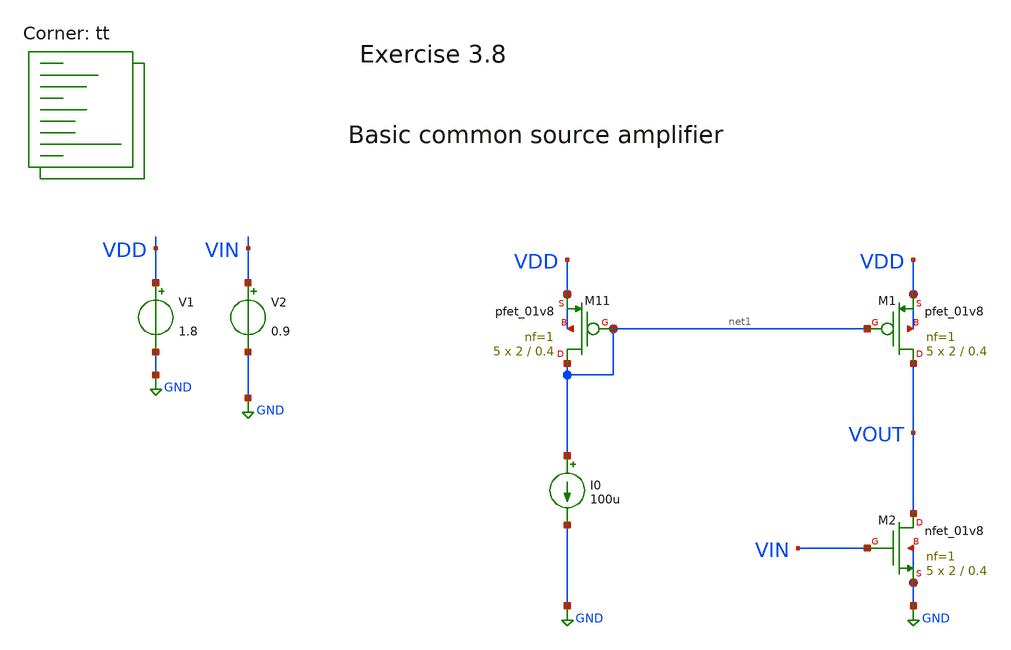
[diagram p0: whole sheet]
** sch_path: Analog_integrated_circuit_Design/chapter3/8/8.sch
**.subckt 8
V1 VDD GND 1.8
V2 VIN GND 0.9
XM11 net1 net1 VDD VDD sky130_fd_pr__pfet_01v8 L=0.4 W=2 nf=1 ad='int((nf+1)/2) * W/nf * 0.29' as='int((nf+2)/2) * W/nf * 0.29'
+ pd='2*int((nf+1)/2) * (W/nf + 0.29)' ps='2*int((nf+2)/2) * (W/nf + 0.29)' nrd='0.29 / W' nrs='0.29 / W'
+ sa=0 sb=0 sd=0 mult=5 m=5
I0 net1 GND 100u
XM1 VOUT net1 VDD VDD sky130_fd_pr__pfet_01v8 L=0.4 W=2 nf=1 ad='int((nf+1)/2) * W/nf * 0.29' as='int((nf+2)/2) * W/nf * 0.29'
+ pd='2*int((nf+1)/2) * (W/nf + 0.29)' ps='2*int((nf+2)/2) * (W/nf + 0.29)' nrd='0.29 / W' nrs='0.29 / W'
+ sa=0 sb=0 sd=0 mult=5 m=5
XM2 VOUT VIN GND GND sky130_fd_pr__nfet_01v8 L=0.4 W=2 nf=1 ad='int((1 + 1)/2) * 2 / 1 * 0.29' as='int((1 + 2)/2) * 2 / 1 * 0.29'
+ pd='2*int((1 + 1)/2) * (2 / 1 + 0.29)' ps='2*int((1 + 2)/2) * (2 / 1 + 0.29)' nrd='0.29 / 2 ' nrs='0.29 / 2 '
+ sa=0 sb=0 sd=0 mult=5 m=5
**** begin user architecture code
.lib $::SKYWATER_MODELS/sky130.lib.spice tt

**************************************************************
**************************************************************
**************************************************************
**************************************************************
**************************************************************
*LIBs*********************************************************
**************************************************************
**************************************************************
**************************************************************
**************************************************************
**************************************************************
*.lib $::SKYWATER_MODELS/sky130.lib.spice tt
* chose the corners in the corner file
* tt_mm for mismatch
* ss ff sf fs standart corners
* ll hh lh hl capacitor and resistors corners
* mc for total process variation including corners
**************************************************************
**************************************************************
**************************************************************
**************************************************************
**************************************************************
*Corners/montecarlo options***********************************
**************************************************************
**************************************************************
**************************************************************
**************************************************************
**************************************************************
.TEMP 27
**************************************************************
**************************************************************
**************************************************************
**************************************************************
*SIMULATION and Plots*****************************************
**************************************************************
**************************************************************
**************************************************************
**************************************************************
.control
save all
dc V2 0 1.8 0.001
*dc simulation
plot deriv(V(Vout)) v(VOUT)
.endc

**** end user architecture code
**.ends
.GLOBAL GND
.end
